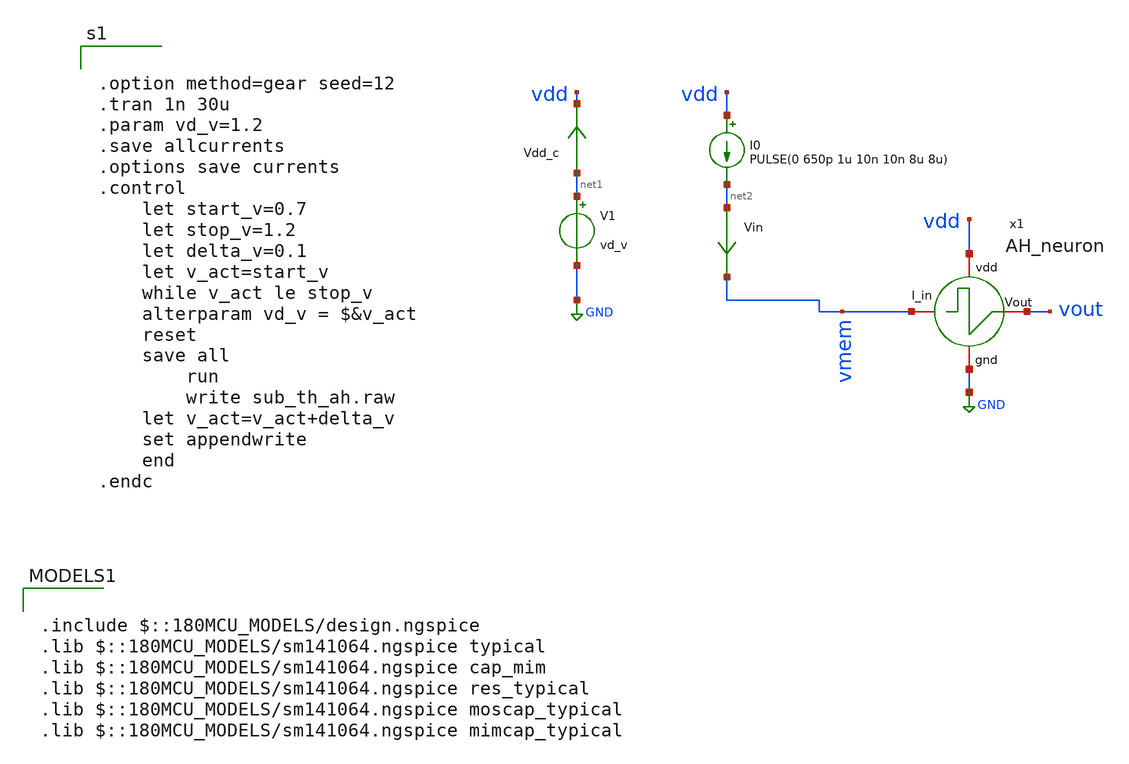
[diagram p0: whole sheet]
** sch_path: designs/libs/tb_AH_neuron/AH_neuron.sch
**.subckt AH_neuron
V1 net1 GND vd_v
Vdd_c net1 vdd 0
.save i(vdd_c)
I0 vdd net2 PULSE(0 650p 1u 10n 10n 8u 8u)
Vin net2 vmem 0
.save i(vin)
x1 vdd vmem vout GND AH_neuron
**** begin user architecture code


.option method=gear seed=12
.tran 1n 30u
.param vd_v=1.2
.save allcurrents
.options save currents
.control
    let start_v=0.7
    let stop_v=1.2
    let delta_v=0.1
    let v_act=start_v
    while v_act le stop_v
	alterparam vd_v = $&v_act
	reset
	save all
        run
        write sub_th_ah.raw
	let v_act=v_act+delta_v
	set appendwrite
    end
.endc



.include $::180MCU_MODELS/design.ngspice
.lib $::180MCU_MODELS/sm141064.ngspice typical
.lib $::180MCU_MODELS/sm141064.ngspice cap_mim
.lib $::180MCU_MODELS/sm141064.ngspice res_typical
.lib $::180MCU_MODELS/sm141064.ngspice moscap_typical
.lib $::180MCU_MODELS/sm141064.ngspice mimcap_typical

**** end user architecture code
**.ends

* expanding   symbol:  designs/libs/core_AH_neuron/AH_neuron.sym # of pins=4
** sym_path: designs/libs/core_AH_neuron/AH_neuron.sym
** sch_path: designs/libs/core_AH_neuron/AH_neuron.sch
.subckt AH_neuron vdd Current_in Vout gnd
*.iopin vdd
*.iopin gnd
*.iopin Current_in
*.iopin Vout
XM5 net1 Current_in vdd vdd pfet_03v3 L=0.28u W=0.22u nf=1 ad='int((nf+1)/2) * W/nf * 0.18u' as='int((nf+2)/2) * W/nf * 0.18u'
+ pd='2*int((nf+1)/2) * (W/nf + 0.18u)' ps='2*int((nf+2)/2) * (W/nf + 0.18u)' nrd='0.18u / W' nrs='0.18u / W'
+ sa=0 sb=0 sd=0 m=1
XM1 Vout net1 vdd vdd pfet_03v3 L=0.28u W=0.22u nf=1 ad='int((nf+1)/2) * W/nf * 0.18u' as='int((nf+2)/2) * W/nf * 0.18u'
+ pd='2*int((nf+1)/2) * (W/nf + 0.18u)' ps='2*int((nf+2)/2) * (W/nf + 0.18u)' nrd='0.18u / W' nrs='0.18u / W'
+ sa=0 sb=0 sd=0 m=1
XM2 net1 Current_in gnd gnd nfet_03v3 L=0.28u W=0.22u nf=1 ad='int((nf+1)/2) * W/nf * 0.18u' as='int((nf+2)/2) * W/nf * 0.18u'
+ pd='2*int((nf+1)/2) * (W/nf + 0.18u)' ps='2*int((nf+2)/2) * (W/nf + 0.18u)' nrd='0.18u / W' nrs='0.18u / W'
+ sa=0 sb=0 sd=0 m=1
XM3 Vout net1 gnd gnd nfet_03v3 L=0.28u W=0.22u nf=1 ad='int((nf+1)/2) * W/nf * 0.18u' as='int((nf+2)/2) * W/nf * 0.18u'
+ pd='2*int((nf+1)/2) * (W/nf + 0.18u)' ps='2*int((nf+2)/2) * (W/nf + 0.18u)' nrd='0.18u / W' nrs='0.18u / W'
+ sa=0 sb=0 sd=0 m=1
XM4 Current_in vgl gnd gnd nfet_03v3 L=2.8u W=0.22u nf=1 ad='int((nf+1)/2) * W/nf * 0.18u' as='int((nf+2)/2) * W/nf * 0.18u'
+ pd='2*int((nf+1)/2) * (W/nf + 0.18u)' ps='2*int((nf+2)/2) * (W/nf + 0.18u)' nrd='0.18u / W' nrs='0.18u / W'
+ sa=0 sb=0 sd=0 m=1
XC1 Current_in Vout cap_mim_1f0fF c_width=1e-6 c_length=1e-6 m=3
XC2 Vout vgl cap_mim_1f0fF c_width=1e-6 c_length=1e-6 m=1
.ends

.GLOBAL GND
.end
